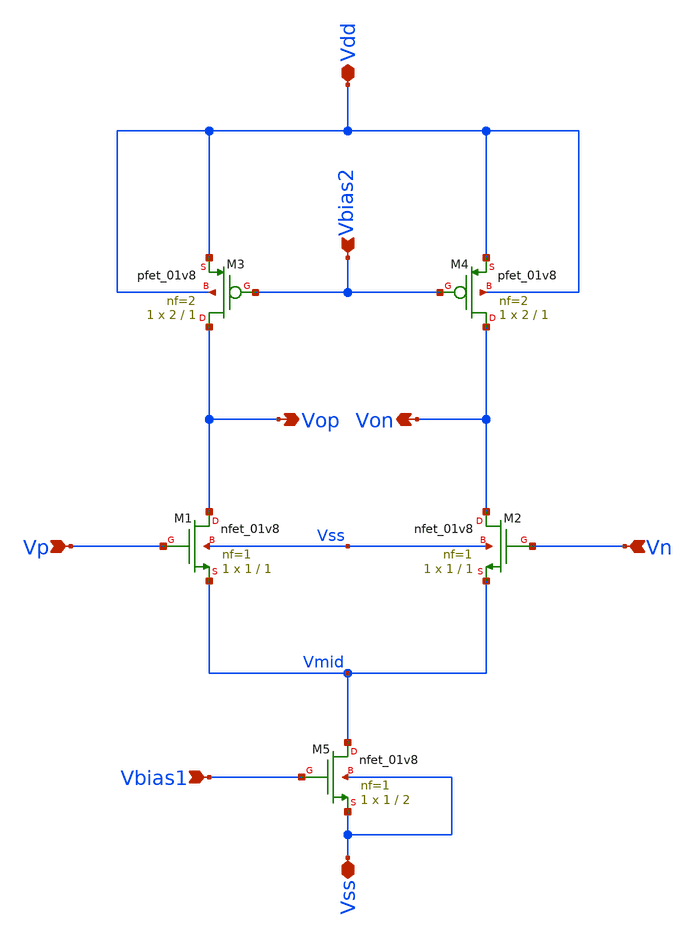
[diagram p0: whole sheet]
** sch_path: Circuits/MillerOpAmpCMMFB/DiffAmp.sch
**.subckt DiffAmp Vdd Vss Vp Vn Vbias1 Vbias2 Vop Von
*.iopin Vdd
*.iopin Vss
*.ipin Vp
*.ipin Vn
*.ipin Vbias1
*.ipin Vbias2
*.opin Vop
*.opin Von
XM1 Vop Vp Vmid Vss sky130_fd_pr__nfet_01v8 L=1 W=1 nf=1 ad='int((nf+1)/2) * W/nf * 0.29' as='int((nf+2)/2) * W/nf * 0.29'
+ pd='2*int((nf+1)/2) * (W/nf + 0.29)' ps='2*int((nf+2)/2) * (W/nf + 0.29)' nrd='0.29 / W' nrs='0.29 / W'
+ sa=0 sb=0 sd=0 mult=1 m=1
XM2 Von Vn Vmid Vss sky130_fd_pr__nfet_01v8 L=1 W=1 nf=1 ad='int((nf+1)/2) * W/nf * 0.29' as='int((nf+2)/2) * W/nf * 0.29'
+ pd='2*int((nf+1)/2) * (W/nf + 0.29)' ps='2*int((nf+2)/2) * (W/nf + 0.29)' nrd='0.29 / W' nrs='0.29 / W'
+ sa=0 sb=0 sd=0 mult=1 m=1
XM3 Vop Vbias2 Vdd Vdd sky130_fd_pr__pfet_01v8 L=1 W=2 nf=2 ad='int((nf+1)/2) * W/nf * 0.29' as='int((nf+2)/2) * W/nf * 0.29'
+ pd='2*int((nf+1)/2) * (W/nf + 0.29)' ps='2*int((nf+2)/2) * (W/nf + 0.29)' nrd='0.29 / W' nrs='0.29 / W'
+ sa=0 sb=0 sd=0 mult=1 m=1
XM4 Von Vbias2 Vdd Vdd sky130_fd_pr__pfet_01v8 L=1 W=2 nf=2 ad='int((nf+1)/2) * W/nf * 0.29' as='int((nf+2)/2) * W/nf * 0.29'
+ pd='2*int((nf+1)/2) * (W/nf + 0.29)' ps='2*int((nf+2)/2) * (W/nf + 0.29)' nrd='0.29 / W' nrs='0.29 / W'
+ sa=0 sb=0 sd=0 mult=1 m=1
XM5 Vmid Vbias1 Vss Vss sky130_fd_pr__nfet_01v8 L=2 W=1 nf=1 ad='int((nf+1)/2) * W/nf * 0.29' as='int((nf+2)/2) * W/nf * 0.29'
+ pd='2*int((nf+1)/2) * (W/nf + 0.29)' ps='2*int((nf+2)/2) * (W/nf + 0.29)' nrd='0.29 / W' nrs='0.29 / W'
+ sa=0 sb=0 sd=0 mult=1 m=1
**.ends
.end
